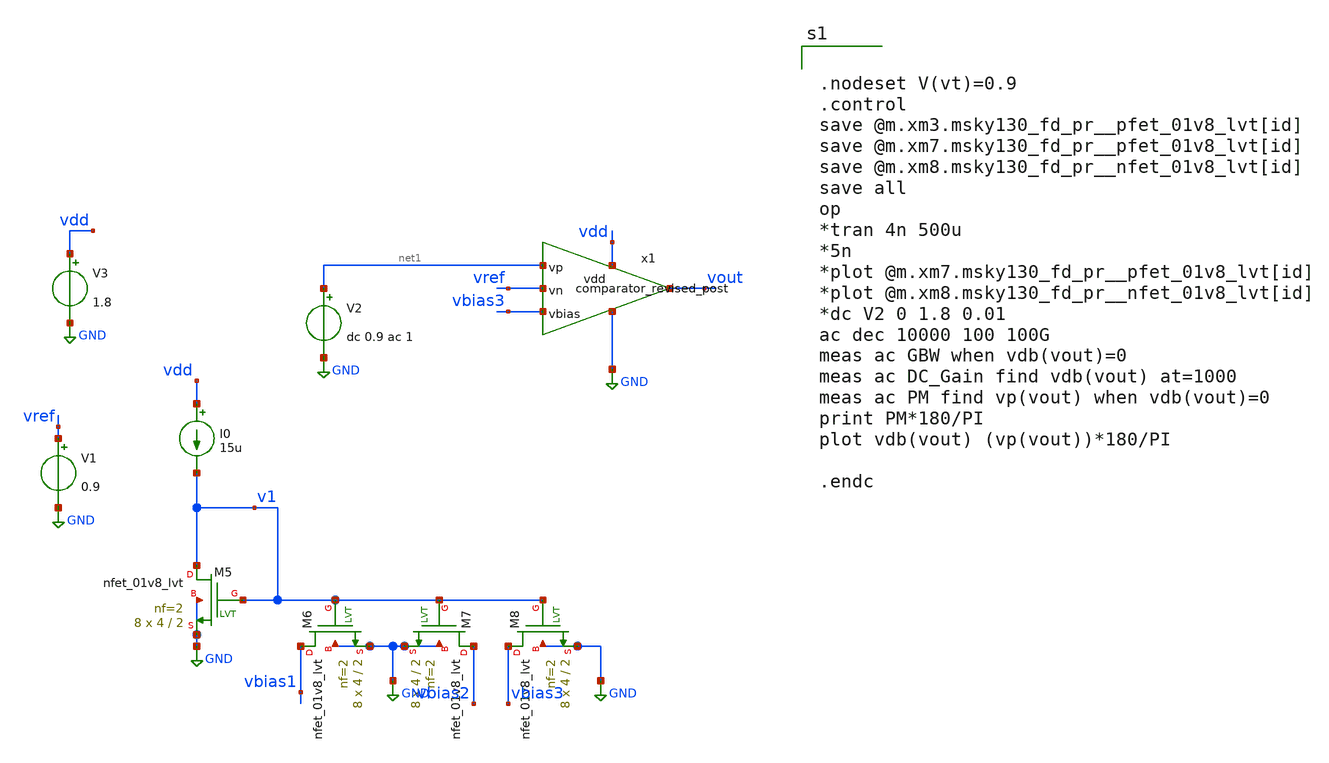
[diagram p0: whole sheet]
** sch_path: xschem/src/comparator/comparator_tb.sch
**.subckt comparator_tb
V3 vdd GND 1.8
V1 vref GND 0.9
I0 vdd v1 15u
XM5 v1 v1 GND GND sky130_fd_pr__nfet_01v8_lvt L=2 W=4 nf=2 ad='int((nf+1)/2) * W/nf * 0.29' as='int((nf+2)/2) * W/nf * 0.29'
+ pd='2*int((nf+1)/2) * (W/nf + 0.29)' ps='2*int((nf+2)/2) * (W/nf + 0.29)' nrd='0.29 / W' nrs='0.29 / W'
+ sa=0 sb=0 sd=0 mult=8 m=8
XM6 vbias1 v1 GND GND sky130_fd_pr__nfet_01v8_lvt L=2 W=4 nf=2 ad='int((nf+1)/2) * W/nf * 0.29' as='int((nf+2)/2) * W/nf * 0.29'
+ pd='2*int((nf+1)/2) * (W/nf + 0.29)' ps='2*int((nf+2)/2) * (W/nf + 0.29)' nrd='0.29 / W' nrs='0.29 / W'
+ sa=0 sb=0 sd=0 mult=8 m=8
XM7 vbias2 v1 GND GND sky130_fd_pr__nfet_01v8_lvt L=2 W=4 nf=2 ad='int((nf+1)/2) * W/nf * 0.29' as='int((nf+2)/2) * W/nf * 0.29'
+ pd='2*int((nf+1)/2) * (W/nf + 0.29)' ps='2*int((nf+2)/2) * (W/nf + 0.29)' nrd='0.29 / W' nrs='0.29 / W'
+ sa=0 sb=0 sd=0 mult=8 m=8
XM8 vbias3 v1 GND GND sky130_fd_pr__nfet_01v8_lvt L=2 W=4 nf=2 ad='int((nf+1)/2) * W/nf * 0.29' as='int((nf+2)/2) * W/nf * 0.29'
+ pd='2*int((nf+1)/2) * (W/nf + 0.29)' ps='2*int((nf+2)/2) * (W/nf + 0.29)' nrd='0.29 / W' nrs='0.29 / W'
+ sa=0 sb=0 sd=0 mult=8 m=8
x1 vdd net1 vref vbias3 GND vout comparator_revised_post
V2 net1 GND dc 0.9 ac 1
**** begin user architecture code


.nodeset V(vt)=0.9
.control
save @m.xm3.msky130_fd_pr__pfet_01v8_lvt[id]
save @m.xm7.msky130_fd_pr__pfet_01v8_lvt[id]
save @m.xm8.msky130_fd_pr__nfet_01v8_lvt[id]
save all
op
*tran 4n 500u
*5n
*plot @m.xm7.msky130_fd_pr__pfet_01v8_lvt[id]
*plot @m.xm8.msky130_fd_pr__nfet_01v8_lvt[id]
*dc V2 0 1.8 0.01
ac dec 10000 100 100G
meas ac GBW when vdb(vout)=0
meas ac DC_Gain find vdb(vout) at=1000
meas ac PM find vp(vout) when vdb(vout)=0
print PM*180/PI
plot vdb(vout) (vp(vout))*180/PI

.endc



.include /home/eda/pdk/skywater-pdk/libraries/sky130_fd_pr_ngspice/latest/models/corners/tt.spice
.include /home/eda/magic/class_d_audio_amplifier/comparator/comparator_post.spice

.include /home/eda/magic/class_d_audio_amplifier/comparator/comparator_revised_post.spice
* Resistor$::SKYWATER_MODELS/Capacitor
.include $::SKYWATER_MODELS/models/r+c/res_typical__cap_typical.spice
.include $::SKYWATER_MODELS/models/r+c/res_typical__cap_typical__lin.spice
* Special cells
.include $::SKYWATER_MODELS/models/corners/tt/specialized_cells.spice


**** end user architecture code
**.ends
.GLOBAL GND
.end
